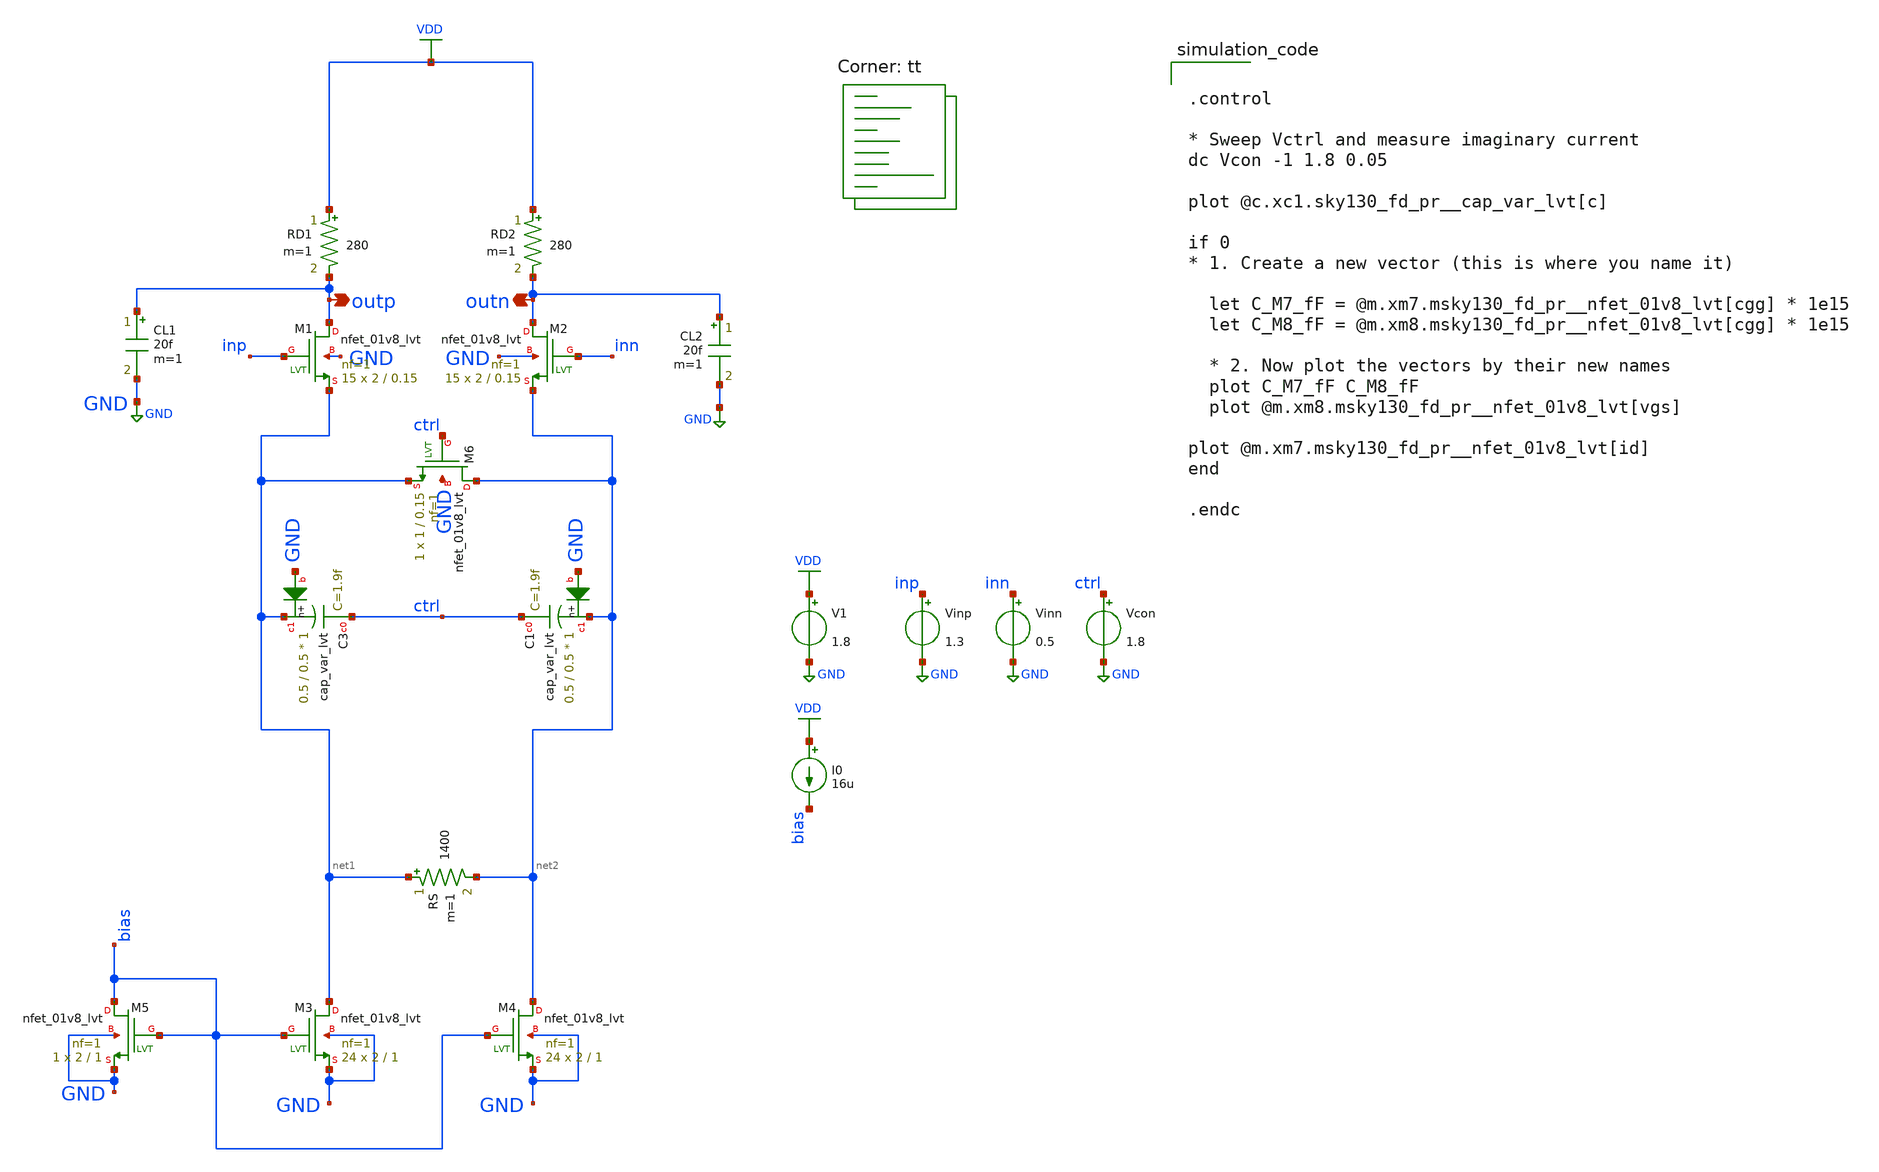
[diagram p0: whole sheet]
** sch_path: CTLE/ctle_sym_adaptive_cap.sch
**.subckt ctle_sym_adaptive_cap outp outn
*.opin outp
*.opin outn
XM1 outp inp net1 GND sky130_fd_pr__nfet_01v8_lvt L=0.15 W=2 nf=1 ad='int((nf+1)/2) * W/nf * 0.29' as='int((nf+2)/2) * W/nf * 0.29'
+ pd='2*int((nf+1)/2) * (W/nf + 0.29)' ps='2*int((nf+2)/2) * (W/nf + 0.29)' nrd='0.29 / W' nrs='0.29 / W'
+ sa=0 sb=0 sd=0 mult=15 m=15
XM2 outn inn net2 GND sky130_fd_pr__nfet_01v8_lvt L=0.15 W=2 nf=1 ad='int((nf+1)/2) * W/nf * 0.29' as='int((nf+2)/2) * W/nf * 0.29'
+ pd='2*int((nf+1)/2) * (W/nf + 0.29)' ps='2*int((nf+2)/2) * (W/nf + 0.29)' nrd='0.29 / W' nrs='0.29 / W'
+ sa=0 sb=0 sd=0 mult=15 m=15
XM3 net1 bias GND GND sky130_fd_pr__nfet_01v8_lvt L=1 W=2 nf=1 ad='int((nf+1)/2) * W/nf * 0.29' as='int((nf+2)/2) * W/nf * 0.29'
+ pd='2*int((nf+1)/2) * (W/nf + 0.29)' ps='2*int((nf+2)/2) * (W/nf + 0.29)' nrd='0.29 / W' nrs='0.29 / W'
+ sa=0 sb=0 sd=0 mult=24 m=24
XM4 net2 bias GND GND sky130_fd_pr__nfet_01v8_lvt L=1 W=2 nf=1 ad='int((nf+1)/2) * W/nf * 0.29' as='int((nf+2)/2) * W/nf * 0.29'
+ pd='2*int((nf+1)/2) * (W/nf + 0.29)' ps='2*int((nf+2)/2) * (W/nf + 0.29)' nrd='0.29 / W' nrs='0.29 / W'
+ sa=0 sb=0 sd=0 mult=24 m=24
XM5 bias bias GND GND sky130_fd_pr__nfet_01v8_lvt L=1 W=2 nf=1 ad='int((nf+1)/2) * W/nf * 0.29' as='int((nf+2)/2) * W/nf * 0.29'
+ pd='2*int((nf+1)/2) * (W/nf + 0.29)' ps='2*int((nf+2)/2) * (W/nf + 0.29)' nrd='0.29 / W' nrs='0.29 / W'
+ sa=0 sb=0 sd=0 mult=1 m=1
RD1 VDD outp 280 m=1
RD2 VDD outn 280 m=1
RS net1 net2 1400 m=1
CL1 outp GND 20f m=1
CL2 outn GND 20f m=1
XM6 net2 ctrl net1 GND sky130_fd_pr__nfet_01v8_lvt L=0.15 W=1 nf=1 ad='int((nf+1)/2) * W/nf * 0.29' as='int((nf+2)/2) * W/nf * 0.29'
+ pd='2*int((nf+1)/2) * (W/nf + 0.29)' ps='2*int((nf+2)/2) * (W/nf + 0.29)' nrd='0.29 / W' nrs='0.29 / W'
+ sa=0 sb=0 sd=0 mult=1 m=1
V1 VDD GND 1.8
Vinp inp GND 1.3
Vinn inn GND 0.5
Vcon ctrl GND 1.8
I0 VDD bias 16u
XC3 ctrl net1 GND sky130_fd_pr__cap_var_lvt W=0.5 L=0.5 VM=1 m=1
XC1 ctrl net2 GND sky130_fd_pr__cap_var_lvt W=0.5 L=0.5 VM=1 m=1
**** begin user architecture code
.lib $::SKYWATER_MODELS/sky130.lib.spice tt


.control

* Sweep Vctrl and measure imaginary current
dc Vcon -1 1.8 0.05

plot @c.xc1.sky130_fd_pr__cap_var_lvt[c]

if 0
* 1. Create a new vector (this is where you name it)

  let C_M7_fF = @m.xm7.msky130_fd_pr__nfet_01v8_lvt[cgg] * 1e15
  let C_M8_fF = @m.xm8.msky130_fd_pr__nfet_01v8_lvt[cgg] * 1e15

  * 2. Now plot the vectors by their new names
  plot C_M7_fF C_M8_fF
  plot @m.xm8.msky130_fd_pr__nfet_01v8_lvt[vgs]

plot @m.xm7.msky130_fd_pr__nfet_01v8_lvt[id]
end

.endc


**** end user architecture code
**.ends
.GLOBAL GND
.GLOBAL VDD
.end
